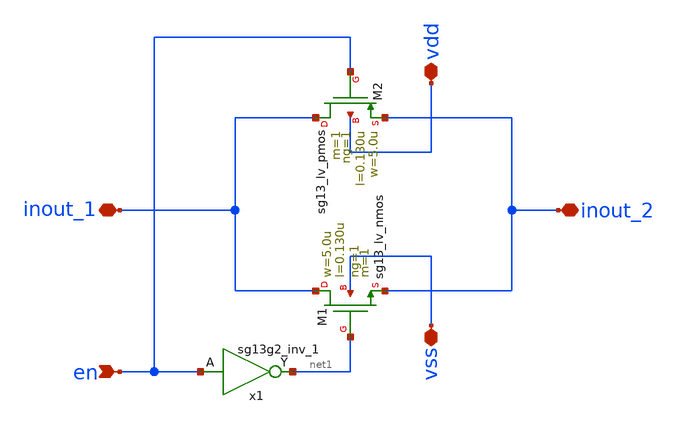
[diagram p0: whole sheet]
** sch_path: ts_pr_May2024/design_data/xschem/transmission_gate_v1.sch
**.subckt transmission_gate_v1 inout_1 inout_2 en vdd vss
*.iopin inout_1
*.iopin inout_2
*.ipin en
*.iopin vdd
*.iopin vss
x1 net1 en VDD VSS sg13g2_inv_1
XM1 inout_1 net1 inout_2 vss sg13_lv_nmos w=5.0u l=0.130u ng=1 m=1 mm_ok=1
XM2 inout_1 en inout_2 vdd sg13_lv_pmos w=5.0u l=0.130u ng=1 m=1 mm_ok=1
**.ends

* expanding   symbol:  sg13g2_stdcells-dev/sg13g2_inv_1.sym # of pins=2
** sym_path: sg13g2_stdcells-dev/sg13g2_inv_1.sym
** sch_path: sg13g2_stdcells-dev/sg13g2_inv_1.sch
.subckt sg13g2_inv_1 Y A VDD VSS
*.opin Y
*.ipin A
*.iopin VDD
*.iopin VSS
XM1 Y A VSS VSS sg13_lv_nmos w=740.00n l=130.00n ng=1 m=1 mm_ok=1
XM2 Y A VDD VDD sg13_lv_pmos w=1.12u l=130.00n ng=1 m=1 mm_ok=1
.ends

.end
